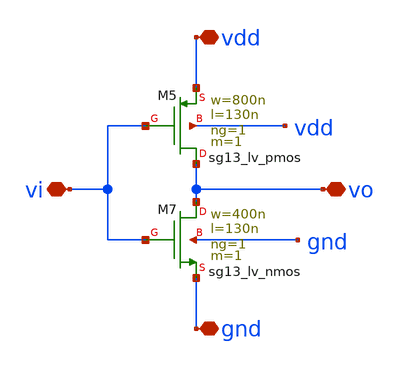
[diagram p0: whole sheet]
** sch_path: modules/module_3_8_bit_SAR_ADC/part_2_digital_comps/bootstrap_switch/schematic/inverter.sch
**.subckt inverter vi vo gnd vdd
*.iopin vi
*.iopin vo
*.iopin gnd
*.iopin vdd
XM5 vo vi vdd vdd sg13_lv_pmos w=800n l=130n ng=1 m=1 mm_ok=1
XM7 vo vi gnd gnd sg13_lv_nmos w=400n l=130n ng=1 m=1 mm_ok=1
**.ends
.end
